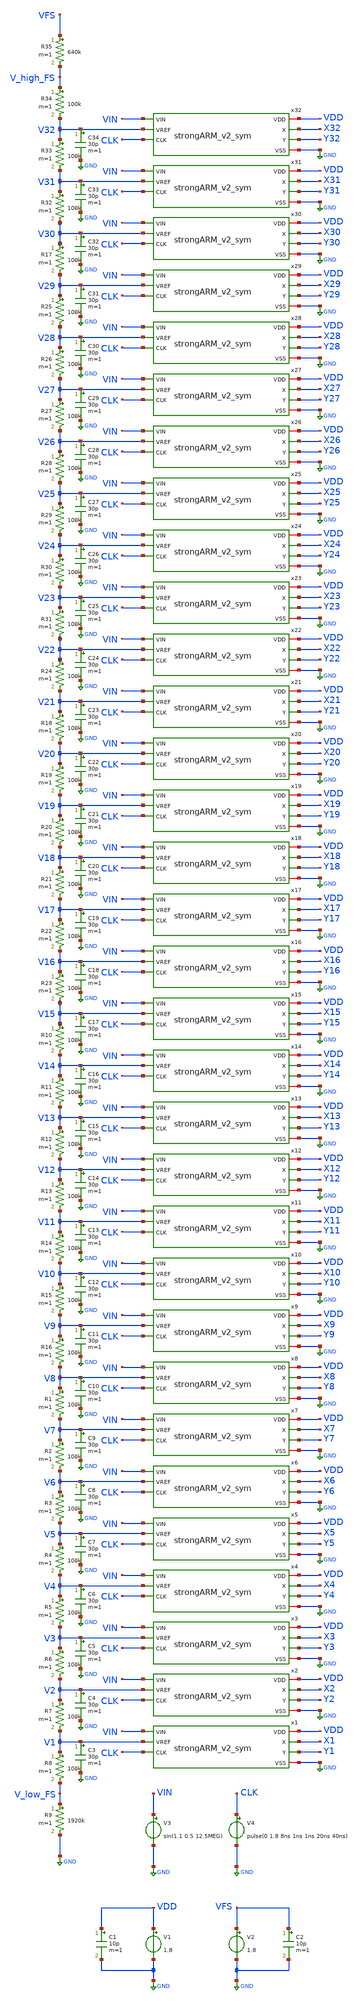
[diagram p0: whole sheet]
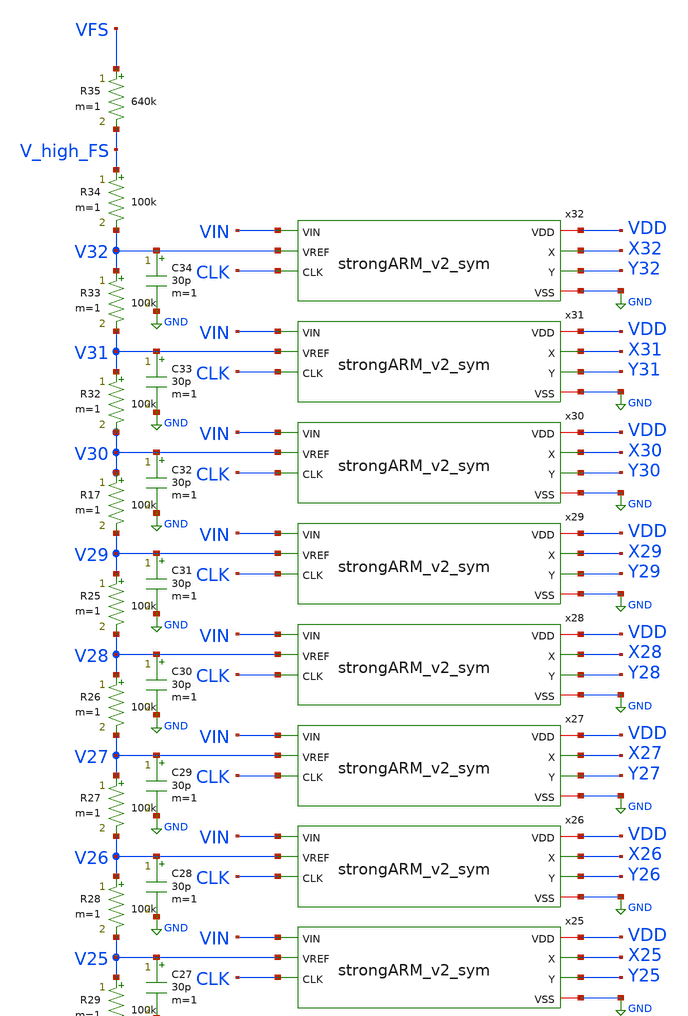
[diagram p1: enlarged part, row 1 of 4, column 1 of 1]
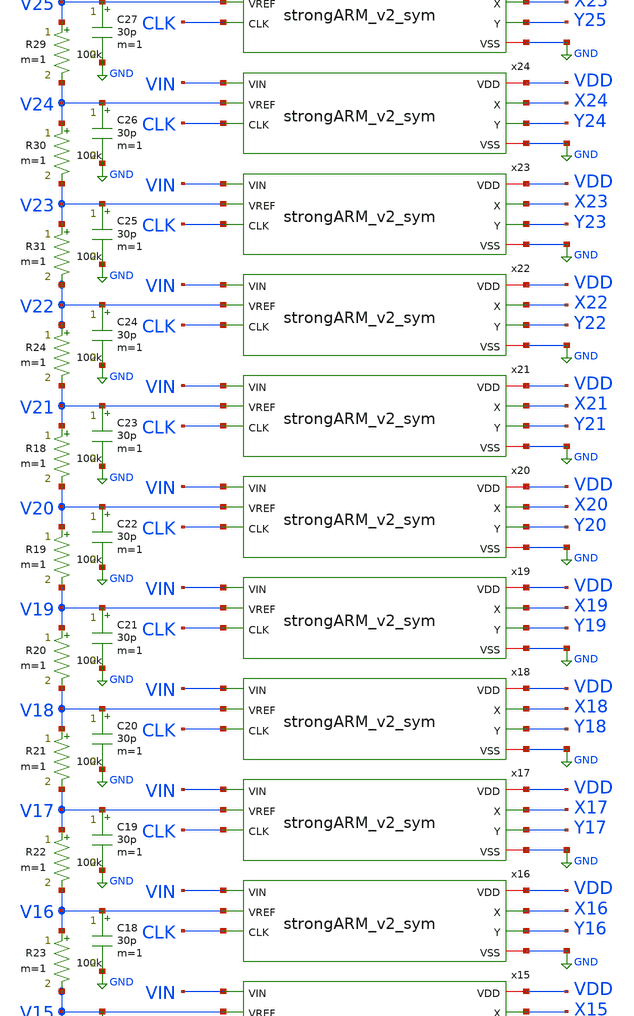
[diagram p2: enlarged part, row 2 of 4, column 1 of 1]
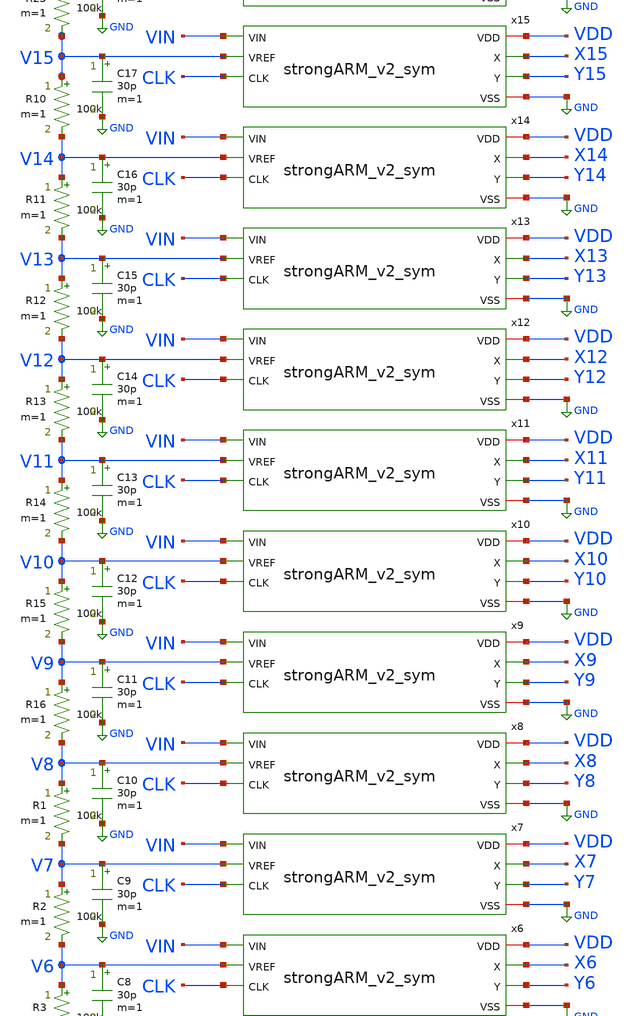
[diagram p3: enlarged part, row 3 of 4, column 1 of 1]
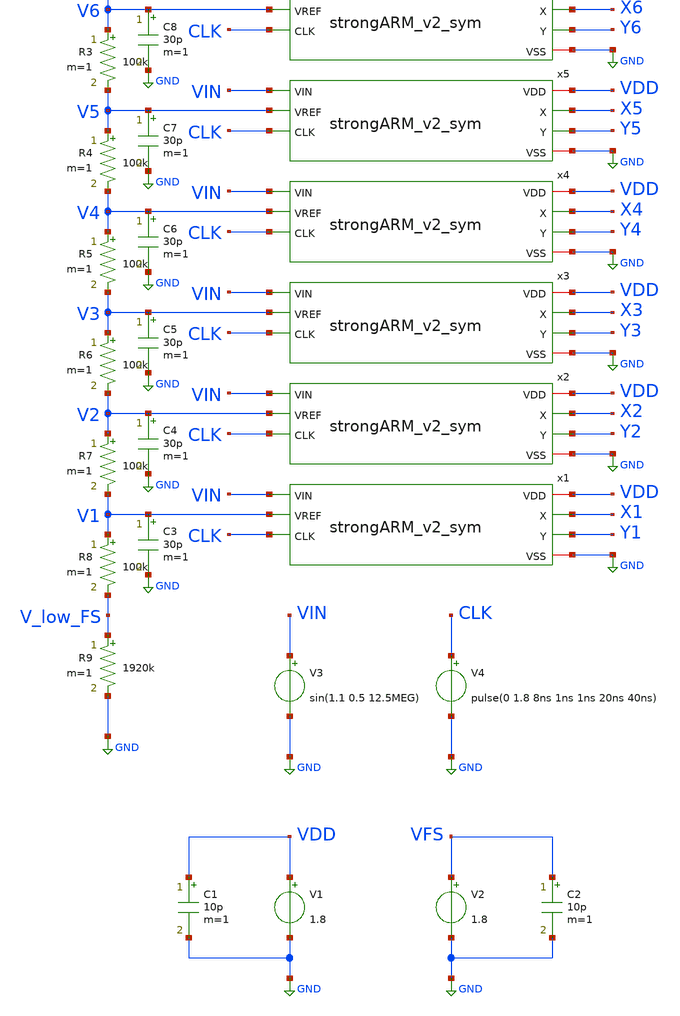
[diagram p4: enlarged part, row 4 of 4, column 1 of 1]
** sch_path: strongARM/flash_ADC_5b.sch
**.subckt flash_ADC_5b
R1 V8 V7 100k m=1
R2 V7 V6 100k m=1
R3 V6 V5 100k m=1
R4 V5 V4 100k m=1
R5 V4 V3 100k m=1
R6 V3 V2 100k m=1
R7 V2 V1 100k m=1
R8 V1 V_low_FS 100k m=1
R9 V_low_FS GND 1920k m=1
R10 V15 V14 100k m=1
R11 V14 V13 100k m=1
R12 V13 V12 100k m=1
R13 V12 V11 100k m=1
R14 V11 V10 100k m=1
R15 V10 V9 100k m=1
R16 V9 V8 100k m=1
R18 V21 V20 100k m=1
R19 V20 V19 100k m=1
R20 V19 V18 100k m=1
R21 V18 V17 100k m=1
R22 V17 V16 100k m=1
R23 V16 V15 100k m=1
R24 V22 V21 100k m=1
R25 V29 V28 100k m=1
R26 V28 V27 100k m=1
R27 V27 V26 100k m=1
R28 V26 V25 100k m=1
R29 V25 V24 100k m=1
R30 V24 V23 100k m=1
R31 V23 V22 100k m=1
R17 V30 V29 100k m=1
R32 V31 V30 100k m=1
R33 V32 V31 100k m=1
R34 V_high_FS V32 100k m=1
R35 VFS V_high_FS 640k m=1
x1 VDD X1 Y1 VIN V1 CLK GND strongARM_v2_sym
x2 VDD X2 Y2 VIN V2 CLK GND strongARM_v2_sym
x3 VDD X3 Y3 VIN V3 CLK GND strongARM_v2_sym
x4 VDD X4 Y4 VIN V4 CLK GND strongARM_v2_sym
x5 VDD X5 Y5 VIN V5 CLK GND strongARM_v2_sym
x6 VDD X6 Y6 VIN V6 CLK GND strongARM_v2_sym
x7 VDD X7 Y7 VIN V7 CLK GND strongARM_v2_sym
x8 VDD X8 Y8 VIN V8 CLK GND strongARM_v2_sym
x9 VDD X9 Y9 VIN V9 CLK GND strongARM_v2_sym
x10 VDD X10 Y10 VIN V10 CLK GND strongARM_v2_sym
x11 VDD X11 Y11 VIN V11 CLK GND strongARM_v2_sym
x12 VDD X12 Y12 VIN V12 CLK GND strongARM_v2_sym
x13 VDD X13 Y13 VIN V13 CLK GND strongARM_v2_sym
x14 VDD X14 Y14 VIN V14 CLK GND strongARM_v2_sym
x15 VDD X15 Y15 VIN V15 CLK GND strongARM_v2_sym
x16 VDD X16 Y16 VIN V16 CLK GND strongARM_v2_sym
x17 VDD X17 Y17 VIN V17 CLK GND strongARM_v2_sym
x18 VDD X18 Y18 VIN V18 CLK GND strongARM_v2_sym
x19 VDD X19 Y19 VIN V19 CLK GND strongARM_v2_sym
x20 VDD X20 Y20 VIN V20 CLK GND strongARM_v2_sym
x21 VDD X21 Y21 VIN V21 CLK GND strongARM_v2_sym
x22 VDD X22 Y22 VIN V22 CLK GND strongARM_v2_sym
x23 VDD X23 Y23 VIN V23 CLK GND strongARM_v2_sym
x24 VDD X24 Y24 VIN V24 CLK GND strongARM_v2_sym
x25 VDD X25 Y25 VIN V25 CLK GND strongARM_v2_sym
x26 VDD X26 Y26 VIN V26 CLK GND strongARM_v2_sym
x27 VDD X27 Y27 VIN V27 CLK GND strongARM_v2_sym
x28 VDD X28 Y28 VIN V28 CLK GND strongARM_v2_sym
x29 VDD X29 Y29 VIN V29 CLK GND strongARM_v2_sym
x30 VDD X30 Y30 VIN V30 CLK GND strongARM_v2_sym
x31 VDD X31 Y31 VIN V31 CLK GND strongARM_v2_sym
x32 VDD X32 Y32 VIN V32 CLK GND strongARM_v2_sym
V3 VIN GND sin(1.1 0.5 12.5MEG)
V4 CLK GND pulse(0 1.8 8ns 1ns 1ns 20ns 40ns)
V1 VDD GND 1.8
V2 VFS GND 1.8
C1 VDD GND 10p m=1
C2 VFS GND 10p m=1
C3 V1 GND 30p m=1
C4 V2 GND 30p m=1
C5 V3 GND 30p m=1
C6 V4 GND 30p m=1
C7 V5 GND 30p m=1
C8 V6 GND 30p m=1
C9 V7 GND 30p m=1
C10 V8 GND 30p m=1
C11 V9 GND 30p m=1
C12 V10 GND 30p m=1
C13 V11 GND 30p m=1
C14 V12 GND 30p m=1
C15 V13 GND 30p m=1
C16 V14 GND 30p m=1
C17 V15 GND 30p m=1
C18 V16 GND 30p m=1
C19 V17 GND 30p m=1
C20 V18 GND 30p m=1
C21 V19 GND 30p m=1
C22 V20 GND 30p m=1
C23 V21 GND 30p m=1
C24 V22 GND 30p m=1
C25 V23 GND 30p m=1
C26 V24 GND 30p m=1
C27 V25 GND 30p m=1
C28 V26 GND 30p m=1
C29 V27 GND 30p m=1
C30 V28 GND 30p m=1
C31 V29 GND 30p m=1
C32 V30 GND 30p m=1
C33 V31 GND 30p m=1
C34 V32 GND 30p m=1
**** begin user architecture code
.lib $::SKYWATER_MODELS/sky130.lib.spice tt


.options savecurrents
.control

save all

tran 0.005n 120n
remzerovec
write flash_ADC_5b.raw

.endc


**** end user architecture code
**.ends

* expanding   symbol:  /foss/designs/Analog_FA23_SP24/strongARM/strongARM_v2_sym.sym # of pins=7
** sym_path: strongARM/strongARM_v2_sym.sym
** sch_path: strongARM/strongARM_v2_sym.sch
.subckt strongARM_v2_sym VDD X Y VIN VREF CLK VSS
*.iopin VDD
*.ipin VIN
*.ipin VREF
*.opin Y
*.opin X
*.iopin VSS
*.ipin CLK
XM4 net2 CLK VDD VDD sky130_fd_pr__pfet_01v8_lvt L=0.35 W=1 nf=1 ad='int((nf+1)/2) * W/nf * 0.29' as='int((nf+2)/2) * W/nf * 0.29'
+ pd='2*int((nf+1)/2) * (W/nf + 0.29)' ps='2*int((nf+2)/2) * (W/nf + 0.29)' nrd='0.29 / W' nrs='0.29 / W'
+ sa=0 sb=0 sd=0 mult=1 m=1
XM1 X CLK VDD VDD sky130_fd_pr__pfet_01v8_lvt L=0.35 W=1 nf=1 ad='int((nf+1)/2) * W/nf * 0.29' as='int((nf+2)/2) * W/nf * 0.29'
+ pd='2*int((nf+1)/2) * (W/nf + 0.29)' ps='2*int((nf+2)/2) * (W/nf + 0.29)' nrd='0.29 / W' nrs='0.29 / W'
+ sa=0 sb=0 sd=0 mult=1 m=1
XM2 Y X VDD VDD sky130_fd_pr__pfet_01v8_lvt L=0.35 W=1 nf=1 ad='int((nf+1)/2) * W/nf * 0.29' as='int((nf+2)/2) * W/nf * 0.29'
+ pd='2*int((nf+1)/2) * (W/nf + 0.29)' ps='2*int((nf+2)/2) * (W/nf + 0.29)' nrd='0.29 / W' nrs='0.29 / W'
+ sa=0 sb=0 sd=0 mult=1 m=1
XM3 X Y VDD VDD sky130_fd_pr__pfet_01v8_lvt L=0.35 W=1 nf=1 ad='int((nf+1)/2) * W/nf * 0.29' as='int((nf+2)/2) * W/nf * 0.29'
+ pd='2*int((nf+1)/2) * (W/nf + 0.29)' ps='2*int((nf+2)/2) * (W/nf + 0.29)' nrd='0.29 / W' nrs='0.29 / W'
+ sa=0 sb=0 sd=0 mult=1 m=1
XM5 Y CLK VDD VDD sky130_fd_pr__pfet_01v8_lvt L=0.35 W=1 nf=1 ad='int((nf+1)/2) * W/nf * 0.29' as='int((nf+2)/2) * W/nf * 0.29'
+ pd='2*int((nf+1)/2) * (W/nf + 0.29)' ps='2*int((nf+2)/2) * (W/nf + 0.29)' nrd='0.29 / W' nrs='0.29 / W'
+ sa=0 sb=0 sd=0 mult=1 m=1
XM6 net3 CLK VDD VDD sky130_fd_pr__pfet_01v8_lvt L=0.35 W=1 nf=1 ad='int((nf+1)/2) * W/nf * 0.29' as='int((nf+2)/2) * W/nf * 0.29'
+ pd='2*int((nf+1)/2) * (W/nf + 0.29)' ps='2*int((nf+2)/2) * (W/nf + 0.29)' nrd='0.29 / W' nrs='0.29 / W'
+ sa=0 sb=0 sd=0 mult=1 m=1
XM10 X Y net2 VSS sky130_fd_pr__nfet_01v8_lvt L=0.15 W=1 nf=1 ad='int((nf+1)/2) * W/nf * 0.29' as='int((nf+2)/2) * W/nf * 0.29'
+ pd='2*int((nf+1)/2) * (W/nf + 0.29)' ps='2*int((nf+2)/2) * (W/nf + 0.29)' nrd='0.29 / W' nrs='0.29 / W'
+ sa=0 sb=0 sd=0 mult=1 m=1
XM7 Y X net3 VSS sky130_fd_pr__nfet_01v8_lvt L=0.15 W=1 nf=1 ad='int((nf+1)/2) * W/nf * 0.29' as='int((nf+2)/2) * W/nf * 0.29'
+ pd='2*int((nf+1)/2) * (W/nf + 0.29)' ps='2*int((nf+2)/2) * (W/nf + 0.29)' nrd='0.29 / W' nrs='0.29 / W'
+ sa=0 sb=0 sd=0 mult=1 m=1
XM8 net2 VIN net1 VSS sky130_fd_pr__nfet_01v8_lvt L=0.15 W=4 nf=1 ad='int((nf+1)/2) * W/nf * 0.29' as='int((nf+2)/2) * W/nf * 0.29'
+ pd='2*int((nf+1)/2) * (W/nf + 0.29)' ps='2*int((nf+2)/2) * (W/nf + 0.29)' nrd='0.29 / W' nrs='0.29 / W'
+ sa=0 sb=0 sd=0 mult=6 m=6
XM9 net3 VREF net1 VSS sky130_fd_pr__nfet_01v8_lvt L=0.15 W=4 nf=1 ad='int((nf+1)/2) * W/nf * 0.29' as='int((nf+2)/2) * W/nf * 0.29'
+ pd='2*int((nf+1)/2) * (W/nf + 0.29)' ps='2*int((nf+2)/2) * (W/nf + 0.29)' nrd='0.29 / W' nrs='0.29 / W'
+ sa=0 sb=0 sd=0 mult=6 m=6
XM11 net1 CLK VSS VSS sky130_fd_pr__nfet_01v8_lvt L=0.15 W=4 nf=1 ad='int((nf+1)/2) * W/nf * 0.29' as='int((nf+2)/2) * W/nf * 0.29'
+ pd='2*int((nf+1)/2) * (W/nf + 0.29)' ps='2*int((nf+2)/2) * (W/nf + 0.29)' nrd='0.29 / W' nrs='0.29 / W'
+ sa=0 sb=0 sd=0 mult=12 m=12
.ends

.GLOBAL GND
.end
